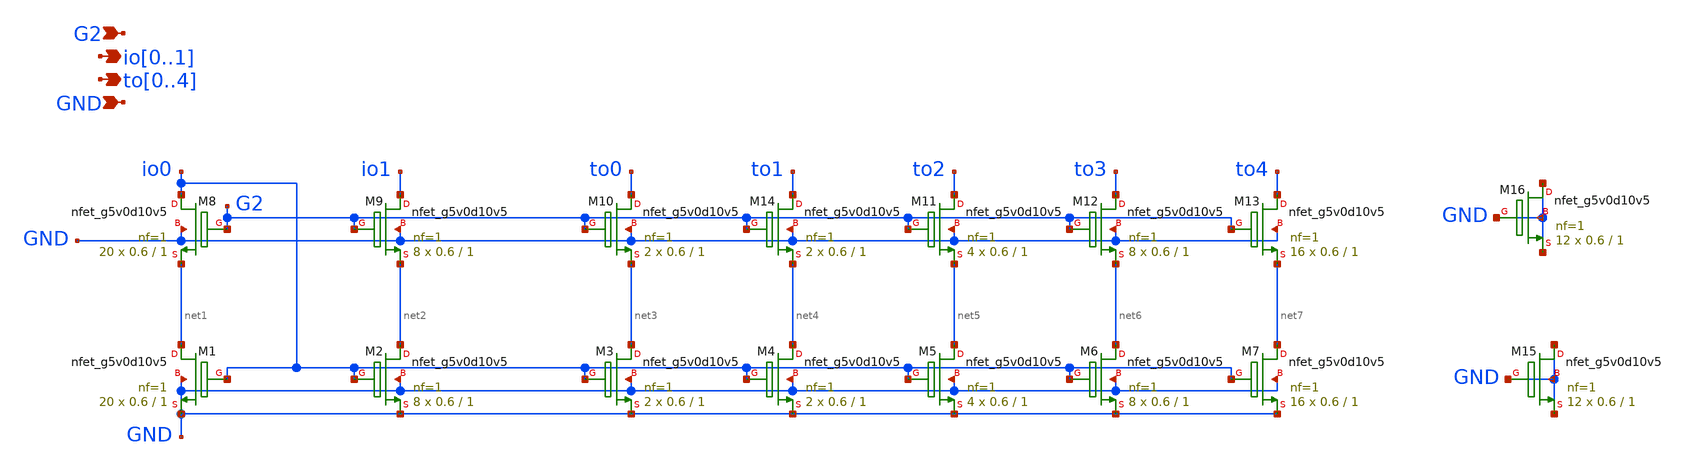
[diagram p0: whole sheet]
** sch_path: xschem/cm_tail.sch
**.subckt cm_tail G2 io0,io1 GND to0,to1,to2,to3,to4
*.ipin G2
*.opin io0,io1
*.ipin GND
*.opin to0,to1,to2,to3,to4
XM1 net1 io0 GND GND sky130_fd_pr__nfet_g5v0d10v5 L=1 W=0.6 nf=1 ad='int((nf+1)/2) * W/nf * 0.29' as='int((nf+2)/2) * W/nf * 0.29'
+ pd='2*int((nf+1)/2) * (W/nf + 0.29)' ps='2*int((nf+2)/2) * (W/nf + 0.29)' nrd='0.29 / W' nrs='0.29 / W'
+ sa=0 sb=0 sd=0 mult=20 m=20
XM2 net2 io0 GND GND sky130_fd_pr__nfet_g5v0d10v5 L=1 W=0.6 nf=1 ad='int((nf+1)/2) * W/nf * 0.29' as='int((nf+2)/2) * W/nf * 0.29'
+ pd='2*int((nf+1)/2) * (W/nf + 0.29)' ps='2*int((nf+2)/2) * (W/nf + 0.29)' nrd='0.29 / W' nrs='0.29 / W'
+ sa=0 sb=0 sd=0 mult=8 m=8
XM3 net3 io0 GND GND sky130_fd_pr__nfet_g5v0d10v5 L=1 W=0.6 nf=1 ad='int((nf+1)/2) * W/nf * 0.29' as='int((nf+2)/2) * W/nf * 0.29'
+ pd='2*int((nf+1)/2) * (W/nf + 0.29)' ps='2*int((nf+2)/2) * (W/nf + 0.29)' nrd='0.29 / W' nrs='0.29 / W'
+ sa=0 sb=0 sd=0 mult=2 m=2
XM5 net5 io0 GND GND sky130_fd_pr__nfet_g5v0d10v5 L=1 W=0.6 nf=1 ad='int((nf+1)/2) * W/nf * 0.29' as='int((nf+2)/2) * W/nf * 0.29'
+ pd='2*int((nf+1)/2) * (W/nf + 0.29)' ps='2*int((nf+2)/2) * (W/nf + 0.29)' nrd='0.29 / W' nrs='0.29 / W'
+ sa=0 sb=0 sd=0 mult=4 m=4
XM6 net6 io0 GND GND sky130_fd_pr__nfet_g5v0d10v5 L=1 W=0.6 nf=1 ad='int((nf+1)/2) * W/nf * 0.29' as='int((nf+2)/2) * W/nf * 0.29'
+ pd='2*int((nf+1)/2) * (W/nf + 0.29)' ps='2*int((nf+2)/2) * (W/nf + 0.29)' nrd='0.29 / W' nrs='0.29 / W'
+ sa=0 sb=0 sd=0 mult=8 m=8
XM7 net7 io0 GND GND sky130_fd_pr__nfet_g5v0d10v5 L=1 W=0.6 nf=1 ad='int((nf+1)/2) * W/nf * 0.29' as='int((nf+2)/2) * W/nf * 0.29'
+ pd='2*int((nf+1)/2) * (W/nf + 0.29)' ps='2*int((nf+2)/2) * (W/nf + 0.29)' nrd='0.29 / W' nrs='0.29 / W'
+ sa=0 sb=0 sd=0 mult=16 m=16
XM4 net4 io0 GND GND sky130_fd_pr__nfet_g5v0d10v5 L=1 W=0.6 nf=1 ad='int((nf+1)/2) * W/nf * 0.29' as='int((nf+2)/2) * W/nf * 0.29'
+ pd='2*int((nf+1)/2) * (W/nf + 0.29)' ps='2*int((nf+2)/2) * (W/nf + 0.29)' nrd='0.29 / W' nrs='0.29 / W'
+ sa=0 sb=0 sd=0 mult=2 m=2
XM8 io0 G2 net1 GND sky130_fd_pr__nfet_g5v0d10v5 L=1 W=0.6 nf=1 ad='int((nf+1)/2) * W/nf * 0.29' as='int((nf+2)/2) * W/nf * 0.29'
+ pd='2*int((nf+1)/2) * (W/nf + 0.29)' ps='2*int((nf+2)/2) * (W/nf + 0.29)' nrd='0.29 / W' nrs='0.29 / W'
+ sa=0 sb=0 sd=0 mult=20 m=20
XM9 io1 G2 net2 GND sky130_fd_pr__nfet_g5v0d10v5 L=1 W=0.6 nf=1 ad='int((nf+1)/2) * W/nf * 0.29' as='int((nf+2)/2) * W/nf * 0.29'
+ pd='2*int((nf+1)/2) * (W/nf + 0.29)' ps='2*int((nf+2)/2) * (W/nf + 0.29)' nrd='0.29 / W' nrs='0.29 / W'
+ sa=0 sb=0 sd=0 mult=8 m=8
XM10 to0 G2 net3 GND sky130_fd_pr__nfet_g5v0d10v5 L=1 W=0.6 nf=1 ad='int((nf+1)/2) * W/nf * 0.29' as='int((nf+2)/2) * W/nf * 0.29'
+ pd='2*int((nf+1)/2) * (W/nf + 0.29)' ps='2*int((nf+2)/2) * (W/nf + 0.29)' nrd='0.29 / W' nrs='0.29 / W'
+ sa=0 sb=0 sd=0 mult=2 m=2
XM11 to2 G2 net5 GND sky130_fd_pr__nfet_g5v0d10v5 L=1 W=0.6 nf=1 ad='int((nf+1)/2) * W/nf * 0.29' as='int((nf+2)/2) * W/nf * 0.29'
+ pd='2*int((nf+1)/2) * (W/nf + 0.29)' ps='2*int((nf+2)/2) * (W/nf + 0.29)' nrd='0.29 / W' nrs='0.29 / W'
+ sa=0 sb=0 sd=0 mult=4 m=4
XM12 to3 G2 net6 GND sky130_fd_pr__nfet_g5v0d10v5 L=1 W=0.6 nf=1 ad='int((nf+1)/2) * W/nf * 0.29' as='int((nf+2)/2) * W/nf * 0.29'
+ pd='2*int((nf+1)/2) * (W/nf + 0.29)' ps='2*int((nf+2)/2) * (W/nf + 0.29)' nrd='0.29 / W' nrs='0.29 / W'
+ sa=0 sb=0 sd=0 mult=8 m=8
XM13 to4 G2 net7 GND sky130_fd_pr__nfet_g5v0d10v5 L=1 W=0.6 nf=1 ad='int((nf+1)/2) * W/nf * 0.29' as='int((nf+2)/2) * W/nf * 0.29'
+ pd='2*int((nf+1)/2) * (W/nf + 0.29)' ps='2*int((nf+2)/2) * (W/nf + 0.29)' nrd='0.29 / W' nrs='0.29 / W'
+ sa=0 sb=0 sd=0 mult=16 m=16
XM14 to1 G2 net4 GND sky130_fd_pr__nfet_g5v0d10v5 L=1 W=0.6 nf=1 ad='int((nf+1)/2) * W/nf * 0.29' as='int((nf+2)/2) * W/nf * 0.29'
+ pd='2*int((nf+1)/2) * (W/nf + 0.29)' ps='2*int((nf+2)/2) * (W/nf + 0.29)' nrd='0.29 / W' nrs='0.29 / W'
+ sa=0 sb=0 sd=0 mult=2 m=2
XM15 GND GND GND GND sky130_fd_pr__nfet_g5v0d10v5 L=1 W=0.6 nf=1 ad='int((nf+1)/2) * W/nf * 0.29' as='int((nf+2)/2) * W/nf * 0.29'
+ pd='2*int((nf+1)/2) * (W/nf + 0.29)' ps='2*int((nf+2)/2) * (W/nf + 0.29)' nrd='0.29 / W' nrs='0.29 / W'
+ sa=0 sb=0 sd=0 mult=12 m=12
XM16 GND GND GND GND sky130_fd_pr__nfet_g5v0d10v5 L=1 W=0.6 nf=1 ad='int((nf+1)/2) * W/nf * 0.29' as='int((nf+2)/2) * W/nf * 0.29'
+ pd='2*int((nf+1)/2) * (W/nf + 0.29)' ps='2*int((nf+2)/2) * (W/nf + 0.29)' nrd='0.29 / W' nrs='0.29 / W'
+ sa=0 sb=0 sd=0 mult=12 m=12
**.ends
.end
